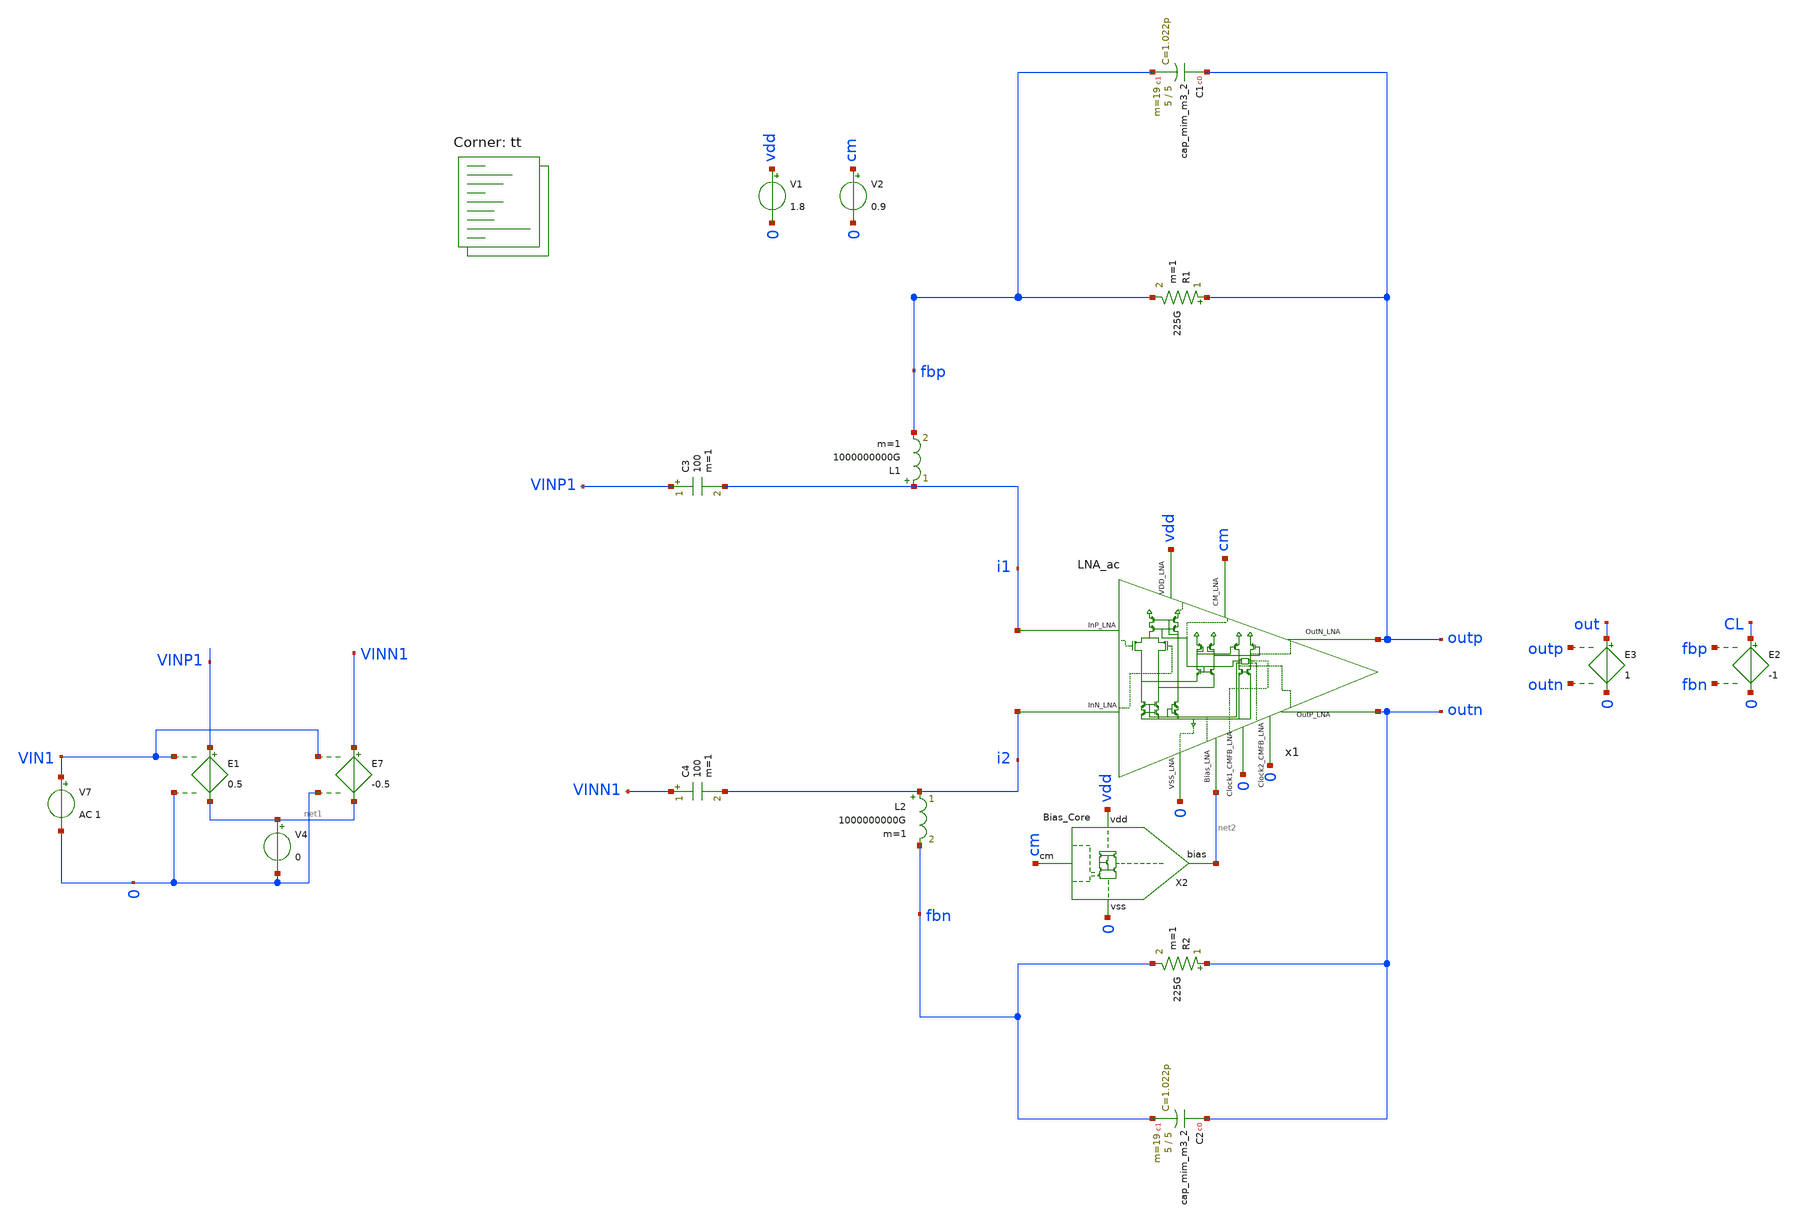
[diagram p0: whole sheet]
** sch_path: testbench_stability.sch
**.subckt testbench_stability
x1 i2 i1 vdd cm outp outn 0 net2 0 0 LNA_ac
V1 vdd 0 1.8
V2 cm 0 0.9
E1 VINP1 net1 VIN1 0 0.5
E7 VINN1 net1 VIN1 0 -0.5
V4 net1 0 0
V7 VIN1 0 AC 1
R1 outp fbp 225G m=1
XC1 outp fbp sky130_fd_pr__cap_mim_m3_2 W=5 L=5 MF=19 m=19
XC2 outn fbn sky130_fd_pr__cap_mim_m3_2 W=5 L=5 MF=19 m=19
R2 outn fbn 225G m=1
X2 cm vdd 0 net2 Bias_Core
E3 out 0 outp outn 1
L1 i1 fbp 1000000000G m=1
L2 i2 fbn 1000000000G m=1
E2 CL 0 fbp fbn -1
C3 VINP1 i1 100 m=1
C4 VINN1 i2 100 m=1
**** begin user architecture code
.lib $::SKYWATER_MODELS/sky130.lib.spice tt


.options savecurrents gmin=1e-25
*ic v(VM5)=0.9 v(VM6)=0.9
.control


save all

save @m.xm11.msky130_fd_pr__pfet_01v8_lvt[id]
save @m.xm11.msky130_fd_pr__pfet_01v8_lvt[vgs]


*nmos
save @m.xm3.msky130_fd_pr__nfet_01v8_lvt[vgs]
save @m.xm3.msky130_fd_pr__nfet_01v8_lvt[vth]
save @m.xm3.msky130_fd_pr__nfet_01v8_lvt[vds]

save @m.xm6.msky130_fd_pr__nfet_01v8_lvt[vgs]
save @m.xm6.msky130_fd_pr__nfet_01v8_lvt[vth]
save @m.xm6.msky130_fd_pr__nfet_01v8_lvt[vds]

save @m.xm8.msky130_fd_pr__nfet_01v8_lvt[vgs]
save @m.xm8.msky130_fd_pr__nfet_01v8_lvt[vth]
save @m.xm8.msky130_fd_pr__nfet_01v8_lvt[vds]

save @m.xm9.msky130_fd_pr__nfet_01v8_lvt[vgs]
save @m.xm9.msky130_fd_pr__nfet_01v8_lvt[vth]
save @m.xm9.msky130_fd_pr__nfet_01v8_lvt[vds]

save @m.xm18.msky130_fd_pr__nfet_01v8_lvt[vgs]
save @m.xm18.msky130_fd_pr__nfet_01v8_lvt[vth]
save @m.xm18.msky130_fd_pr__nfet_01v8_lvt[vds]

save @m.xm19.msky130_fd_pr__nfet_01v8_lvt[vgs]
save @m.xm19.msky130_fd_pr__nfet_01v8_lvt[vth]
save @m.xm19.msky130_fd_pr__nfet_01v8_lvt[vds]

save @m.xm25.msky130_fd_pr__nfet_01v8_lvt[vgs]
save @m.xm25.msky130_fd_pr__nfet_01v8_lvt[vth]
save @m.xm25.msky130_fd_pr__nfet_01v8_lvt[vds]

*pmos

save @m.xm1.msky130_fd_pr__pfet_01v8_lvt[vgs]
save @m.xm1.msky130_fd_pr__pfet_01v8_lvt[vth]
save @m.xm1.msky130_fd_pr__pfet_01v8_lvt[vds]


save @m.xm2.msky130_fd_pr__pfet_01v8_lvt[vgs]
save @m.xm2.msky130_fd_pr__pfet_01v8_lvt[vth]
save @m.xm2.msky130_fd_pr__pfet_01v8_lvt[vds]


save @m.xm10.msky130_fd_pr__pfet_01v8_lvt[vgs]
save @m.xm10.msky130_fd_pr__pfet_01v8_lvt[vth]
save @m.xm10.msky130_fd_pr__pfet_01v8_lvt[vds]

save @m.xm13.msky130_fd_pr__pfet_01v8_lvt[vgs]
save @m.xm13.msky130_fd_pr__pfet_01v8_lvt[vth]
save @m.xm13.msky130_fd_pr__pfet_01v8_lvt[vds]

save @m.xm4.msky130_fd_pr__pfet_01v8_lvt[vgs]
save @m.xm4.msky130_fd_pr__pfet_01v8_lvt[vth]
save @m.xm4.msky130_fd_pr__pfet_01v8_lvt[vds]

save @m.xm5.msky130_fd_pr__pfet_01v8_lvt[vgs]
save @m.xm5.msky130_fd_pr__pfet_01v8_lvt[vth]
save @m.xm5.msky130_fd_pr__pfet_01v8_lvt[vds]

save @m.xm16.msky130_fd_pr__pfet_01v8_lvt[vgs]
save @m.xm16.msky130_fd_pr__pfet_01v8_lvt[vth]
save @m.xm16.msky130_fd_pr__pfet_01v8_lvt[vds]

save @m.xm17.msky130_fd_pr__pfet_01v8_lvt[vgs]
save @m.xm17.msky130_fd_pr__pfet_01v8_lvt[vth]
save @m.xm17.msky130_fd_pr__pfet_01v8_lvt[vds]

save @m.xm3.msky130_fd_pr__pfet_01v8_lvt[vgs]
save @m.xm3.msky130_fd_pr__pfet_01v8_lvt[vth]
save @m.xm3.msky130_fd_pr__pfet_01v8_lvt[vds]

save @m.xm20.msky130_fd_pr__pfet_01v8_lvt[vgs]
save @m.xm20.msky130_fd_pr__pfet_01v8_lvt[vth]
save @m.xm20.msky130_fd_pr__pfet_01v8_lvt[vds]

save @m.xm2.msky130_fd_pr__pfet_01v8_lvt[vgs]
save @m.xm2.msky130_fd_pr__pfet_01v8_lvt[vth]
save @m.xm2.msky130_fd_pr__pfet_01v8_lvt[vds]

save @m.xm21.msky130_fd_pr__pfet_01v8_lvt[vgs]
save @m.xm21.msky130_fd_pr__pfet_01v8_lvt[vth]
save @m.xm21.msky130_fd_pr__pfet_01v8_lvt[vds]

save @m.xm7.msky130_fd_pr__nfet_01v8_lvt[vth]

save @m.xm1.msky130_fd_pr__pfet_01v8[vgs]

save @m.xm1.msky130_fd_pr__nfet_01v8_lvt[gm]


save @m.xm1.msky130_fd_pr__nfet_01v8_lvt[gds]
save @m.xm2.msky130_fd_pr__pfet_01v8_lvt[gm]

save @m.xm23.msky130_fd_pr__nfet_01v8[cgs]
save @m.xm4.msky130_fd_pr__pfet_01v8[cgs]
save @m.xm2.msky130_fd_pr__pfet_01v8_lvt[cgs]



save @m.xm2.msky130_fd_pr__pfet_01v8_lvt[gds]


op
write CL_Stability.raw
*set appendwrite


.endc
.control



*tran 50u 1500m
*save all
*plot v(Outp)-v(outn)


*noise V(Outp,Outn) V7 dec 100 0.1 128
*print inoise_total onoise_total
*setplot noise1
*plot inoise_spectrum

ac dec 10 0.1 1G
let gaind=(v(outp)-v(outn))/(v(in_p1)-v(in_n1))
let lg=fbp-fbn
let BG=(OL/CL)-1
let phase=180*cph(CL)/pi
plot db(gaind)
plot db(CL) phase
plot db(out)

.endc






.include $::SKYWATER_STDCELLS/sky130_fd_sc_hd.spice

**** end user architecture code
**.ends

* expanding   symbol:  LNA/LNA_ac.sym # of pins=10
** sym_path: LNA_ac.sym
** sch_path: LNA_ac.sch
.subckt LNA_ac InN_LNA InP_LNA VDD_LNA CM_LNA OutN_LNA OutP_LNA VSS_LNA Bias_LNA Clock1_CMFB_LNA
+ Clock2_CMFB_LNA
*.iopin InP_LNA
*.iopin InN_LNA
*.iopin VSS_LNA
*.iopin VDD_LNA
*.iopin CM_LNA
*.opin OutP_LNA
*.opin OutN_LNA
*.iopin Clock2_CMFB_LNA
*.iopin Bias_LNA
*.iopin Clock1_CMFB_LNA
XM4 net4 InP_LNA VT2 VT2 sky130_fd_pr__pfet_01v8_lvt L=10 W=10 nf=1 ad='int((nf+1)/2) * W/nf * 0.29'
+ as='int((nf+2)/2) * W/nf * 0.29' pd='2*int((nf+1)/2) * (W/nf + 0.29)' ps='2*int((nf+2)/2) * (W/nf + 0.29)'
+ nrd='0.29 / W' nrs='0.29 / W' sa=0 sb=0 sd=0 mult=45 m=45
XM5 net3 InN_LNA VT2 VT2 sky130_fd_pr__pfet_01v8_lvt L=10 W=10 nf=1 ad='int((nf+1)/2) * W/nf * 0.29'
+ as='int((nf+2)/2) * W/nf * 0.29' pd='2*int((nf+1)/2) * (W/nf + 0.29)' ps='2*int((nf+2)/2) * (W/nf + 0.29)'
+ nrd='0.29 / W' nrs='0.29 / W' sa=0 sb=0 sd=0 mult=45 m=45
XM8 net8 Bias_LNA VSS_LNA VSS_LNA sky130_fd_pr__nfet_01v8_lvt L=20 W=10 nf=1 ad='int((nf+1)/2) * W/nf * 0.29'
+ as='int((nf+2)/2) * W/nf * 0.29' pd='2*int((nf+1)/2) * (W/nf + 0.29)' ps='2*int((nf+2)/2) * (W/nf + 0.29)'
+ nrd='0.29 / W' nrs='0.29 / W' sa=0 sb=0 sd=0 mult=3 m=3
XM9 net9 Bias_LNA VSS_LNA VSS_LNA sky130_fd_pr__nfet_01v8_lvt L=20 W=10 nf=1 ad='int((nf+1)/2) * W/nf * 0.29'
+ as='int((nf+2)/2) * W/nf * 0.29' pd='2*int((nf+1)/2) * (W/nf + 0.29)' ps='2*int((nf+2)/2) * (W/nf + 0.29)'
+ nrd='0.29 / W' nrs='0.29 / W' sa=0 sb=0 sd=0 mult=3 m=3
XM16 net7 b VDD_LNA VDD_LNA sky130_fd_pr__pfet_01v8_lvt L=20 W=6 nf=1 ad='int((nf+1)/2) * W/nf * 0.29'
+ as='int((nf+2)/2) * W/nf * 0.29' pd='2*int((nf+1)/2) * (W/nf + 0.29)' ps='2*int((nf+2)/2) * (W/nf + 0.29)'
+ nrd='0.29 / W' nrs='0.29 / W' sa=0 sb=0 sd=0 mult=1 m=1
XM17 net6 a VDD_LNA VDD_LNA sky130_fd_pr__pfet_01v8_lvt L=20 W=6 nf=1 ad='int((nf+1)/2) * W/nf * 0.29'
+ as='int((nf+2)/2) * W/nf * 0.29' pd='2*int((nf+1)/2) * (W/nf + 0.29)' ps='2*int((nf+2)/2) * (W/nf + 0.29)'
+ nrd='0.29 / W' nrs='0.29 / W' sa=0 sb=0 sd=0 mult=1 m=1
XM18 b CM_LNA net3 VSS_LNA sky130_fd_pr__nfet_01v8_lvt L=20 W=1 nf=1 ad='int((nf+1)/2) * W/nf * 0.29'
+ as='int((nf+2)/2) * W/nf * 0.29' pd='2*int((nf+1)/2) * (W/nf + 0.29)' ps='2*int((nf+2)/2) * (W/nf + 0.29)'
+ nrd='0.29 / W' nrs='0.29 / W' sa=0 sb=0 sd=0 mult=12 m=12
XM19 a CM_LNA net4 VSS_LNA sky130_fd_pr__nfet_01v8_lvt L=20 W=1 nf=1 ad='int((nf+1)/2) * W/nf * 0.29'
+ as='int((nf+2)/2) * W/nf * 0.29' pd='2*int((nf+1)/2) * (W/nf + 0.29)' ps='2*int((nf+2)/2) * (W/nf + 0.29)'
+ nrd='0.29 / W' nrs='0.29 / W' sa=0 sb=0 sd=0 mult=12 m=12
XM20 OutP_LNA a VDD_LNA VDD_LNA sky130_fd_pr__pfet_01v8_lvt L=20 W=6 nf=1 ad='int((nf+1)/2) * W/nf * 0.29'
+ as='int((nf+2)/2) * W/nf * 0.29' pd='2*int((nf+1)/2) * (W/nf + 0.29)' ps='2*int((nf+2)/2) * (W/nf + 0.29)'
+ nrd='0.29 / W' nrs='0.29 / W' sa=0 sb=0 sd=0 mult=10 m=10
XM21 OutN_LNA b VDD_LNA VDD_LNA sky130_fd_pr__pfet_01v8_lvt L=20 W=6 nf=1 ad='int((nf+1)/2) * W/nf * 0.29'
+ as='int((nf+2)/2) * W/nf * 0.29' pd='2*int((nf+1)/2) * (W/nf + 0.29)' ps='2*int((nf+2)/2) * (W/nf + 0.29)'
+ nrd='0.29 / W' nrs='0.29 / W' sa=0 sb=0 sd=0 mult=10 m=10
XM23 OutN_LNA net5 VSS_LNA VSS_LNA sky130_fd_pr__nfet_01v8_lvt L=20 W=10 nf=1 ad='int((nf+1)/2) * W/nf * 0.29'
+ as='int((nf+2)/2) * W/nf * 0.29' pd='2*int((nf+1)/2) * (W/nf + 0.29)' ps='2*int((nf+2)/2) * (W/nf + 0.29)'
+ nrd='0.29 / W' nrs='0.29 / W' sa=0 sb=0 sd=0 mult=10 m=10
XM25 OutP_LNA net5 VSS_LNA VSS_LNA sky130_fd_pr__nfet_01v8_lvt L=20 W=10 nf=1 ad='int((nf+1)/2) * W/nf * 0.29'
+ as='int((nf+2)/2) * W/nf * 0.29' pd='2*int((nf+1)/2) * (W/nf + 0.29)' ps='2*int((nf+2)/2) * (W/nf + 0.29)'
+ nrd='0.29 / W' nrs='0.29 / W' sa=0 sb=0 sd=0 mult=10 m=10
XM2 net10 net1 VDD_LNA VDD_LNA sky130_fd_pr__pfet_01v8_lvt L=10 W=10 nf=1 ad='int((nf+1)/2) * W/nf * 0.29'
+ as='int((nf+2)/2) * W/nf * 0.29' pd='2*int((nf+1)/2) * (W/nf + 0.29)' ps='2*int((nf+2)/2) * (W/nf + 0.29)'
+ nrd='0.29 / W' nrs='0.29 / W' sa=0 sb=0 sd=0 mult=4 m=4
XM3 net11 net1 VDD_LNA VDD_LNA sky130_fd_pr__pfet_01v8_lvt L=10 W=10 nf=1 ad='int((nf+1)/2) * W/nf * 0.29'
+ as='int((nf+2)/2) * W/nf * 0.29' pd='2*int((nf+1)/2) * (W/nf + 0.29)' ps='2*int((nf+2)/2) * (W/nf + 0.29)'
+ nrd='0.29 / W' nrs='0.29 / W' sa=0 sb=0 sd=0 mult=1 m=1
XM6 net2 Bias_LNA VSS_LNA VSS_LNA sky130_fd_pr__nfet_01v8_lvt L=20 W=10 nf=1 ad='int((nf+1)/2) * W/nf * 0.29'
+ as='int((nf+2)/2) * W/nf * 0.29' pd='2*int((nf+1)/2) * (W/nf + 0.29)' ps='2*int((nf+2)/2) * (W/nf + 0.29)'
+ nrd='0.29 / W' nrs='0.29 / W' sa=0 sb=0 sd=0 mult=1 m=1
E3 f1 VSS_LNA OutN_LNA VSS_LNA -1
E4 f2 VSS_LNA OutP_LNA f1 1
E5 f3 VSS_LNA f2 VSS_LNA 0.5
E6 net5 VSS_LNA CM_LNA f3 {-1000}
XC1 OutP_LNA a sky130_fd_pr__cap_mim_m3_2 W=12 L=10 MF=32 m=32
XC2 OutN_LNA b sky130_fd_pr__cap_mim_m3_2 W=12 L=10 MF=32 m=32
XM1 net4 CM_LNA net8 VSS_LNA sky130_fd_pr__nfet_01v8_lvt L=1 W=10 nf=1 ad='int((nf+1)/2) * W/nf * 0.29'
+ as='int((nf+2)/2) * W/nf * 0.29' pd='2*int((nf+1)/2) * (W/nf + 0.29)' ps='2*int((nf+2)/2) * (W/nf + 0.29)'
+ nrd='0.29 / W' nrs='0.29 / W' sa=0 sb=0 sd=0 mult=120 m=120
XM7 net3 CM_LNA net9 VSS_LNA sky130_fd_pr__nfet_01v8_lvt L=1 W=10 nf=1 ad='int((nf+1)/2) * W/nf * 0.29'
+ as='int((nf+2)/2) * W/nf * 0.29' pd='2*int((nf+1)/2) * (W/nf + 0.29)' ps='2*int((nf+2)/2) * (W/nf + 0.29)'
+ nrd='0.29 / W' nrs='0.29 / W' sa=0 sb=0 sd=0 mult=120 m=120
XM10 net1 CM_LNA net2 VSS_LNA sky130_fd_pr__nfet_01v8_lvt L=1 W=10 nf=1 ad='int((nf+1)/2) * W/nf * 0.29'
+ as='int((nf+2)/2) * W/nf * 0.29' pd='2*int((nf+1)/2) * (W/nf + 0.29)' ps='2*int((nf+2)/2) * (W/nf + 0.29)'
+ nrd='0.29 / W' nrs='0.29 / W' sa=0 sb=0 sd=0 mult=40 m=40
XM11 net1 CM_LNA net11 VDD_LNA sky130_fd_pr__pfet_01v8_lvt L=10 W=10 nf=1 ad='int((nf+1)/2) * W/nf * 0.29'
+ as='int((nf+2)/2) * W/nf * 0.29' pd='2*int((nf+1)/2) * (W/nf + 0.29)' ps='2*int((nf+2)/2) * (W/nf + 0.29)'
+ nrd='0.29 / W' nrs='0.29 / W' sa=0 sb=0 sd=0 mult=5 m=5
XM12 VT2 CM_LNA net10 VDD_LNA sky130_fd_pr__pfet_01v8_lvt L=10 W=10 nf=1 ad='int((nf+1)/2) * W/nf * 0.29'
+ as='int((nf+2)/2) * W/nf * 0.29' pd='2*int((nf+1)/2) * (W/nf + 0.29)' ps='2*int((nf+2)/2) * (W/nf + 0.29)'
+ nrd='0.29 / W' nrs='0.29 / W' sa=0 sb=0 sd=0 mult=20 m=20
XM13 b CM_LNA net7 VDD_LNA sky130_fd_pr__pfet_01v8_lvt L=20 W=6 nf=1 ad='int((nf+1)/2) * W/nf * 0.29'
+ as='int((nf+2)/2) * W/nf * 0.29' pd='2*int((nf+1)/2) * (W/nf + 0.29)' ps='2*int((nf+2)/2) * (W/nf + 0.29)'
+ nrd='0.29 / W' nrs='0.29 / W' sa=0 sb=0 sd=0 mult=10 m=10
XM14 a CM_LNA net6 VDD_LNA sky130_fd_pr__pfet_01v8_lvt L=20 W=6 nf=1 ad='int((nf+1)/2) * W/nf * 0.29'
+ as='int((nf+2)/2) * W/nf * 0.29' pd='2*int((nf+1)/2) * (W/nf + 0.29)' ps='2*int((nf+2)/2) * (W/nf + 0.29)'
+ nrd='0.29 / W' nrs='0.29 / W' sa=0 sb=0 sd=0 mult=10 m=10
.ends


* expanding   symbol:  LNA/Bias_Core.sym # of pins=4
** sym_path: Bias_Core.sym
** sch_path: Bias_Core.sch
.subckt Bias_Core cm vdd vss bias
*.ipin vdd
*.ipin vss
*.opin bias
*.ipin cm
XM7 net3 bias vss vss sky130_fd_pr__nfet_01v8_lvt L=20 W=10 nf=1 ad='int((nf+1)/2) * W/nf * 0.29' as='int((nf+2)/2) * W/nf * 0.29'
+ pd='2*int((nf+1)/2) * (W/nf + 0.29)' ps='2*int((nf+2)/2) * (W/nf + 0.29)' nrd='0.29 / W' nrs='0.29 / W'
+ sa=0 sb=0 sd=0 mult=1 m=1
XM10 net4 vx vr vdd sky130_fd_pr__pfet_01v8_lvt L=20 W=10 nf=1 ad='int((nf+1)/2) * W/nf * 0.29' as='int((nf+2)/2) * W/nf * 0.29'
+ pd='2*int((nf+1)/2) * (W/nf + 0.29)' ps='2*int((nf+2)/2) * (W/nf + 0.29)' nrd='0.29 / W' nrs='0.29 / W'
+ sa=0 sb=0 sd=0 mult=20 m=20
XM11 bias cm net3 vss sky130_fd_pr__nfet_01v8_lvt L=20 W=10 nf=1 ad='int((nf+1)/2) * W/nf * 0.29' as='int((nf+2)/2) * W/nf * 0.29'
+ pd='2*int((nf+1)/2) * (W/nf + 0.29)' ps='2*int((nf+2)/2) * (W/nf + 0.29)' nrd='0.29 / W' nrs='0.29 / W'
+ sa=0 sb=0 sd=0 mult=40 m=40
XM12 net2 bias vss vss sky130_fd_pr__nfet_01v8_lvt L=20 W=10 nf=1 ad='int((nf+1)/2) * W/nf * 0.29' as='int((nf+2)/2) * W/nf * 0.29'
+ pd='2*int((nf+1)/2) * (W/nf + 0.29)' ps='2*int((nf+2)/2) * (W/nf + 0.29)' nrd='0.29 / W' nrs='0.29 / W'
+ sa=0 sb=0 sd=0 mult=1 m=1
XM13 vx cm net2 vss sky130_fd_pr__nfet_01v8_lvt L=20 W=10 nf=1 ad='int((nf+1)/2) * W/nf * 0.29' as='int((nf+2)/2) * W/nf * 0.29'
+ pd='2*int((nf+1)/2) * (W/nf + 0.29)' ps='2*int((nf+2)/2) * (W/nf + 0.29)' nrd='0.29 / W' nrs='0.29 / W'
+ sa=0 sb=0 sd=0 mult=40 m=40
XM2 net8 vx net1 vdd sky130_fd_pr__pfet_01v8_lvt L=20 W=10 nf=1 ad='int((nf+1)/2) * W/nf * 0.29' as='int((nf+2)/2) * W/nf * 0.29'
+ pd='2*int((nf+1)/2) * (W/nf + 0.29)' ps='2*int((nf+2)/2) * (W/nf + 0.29)' nrd='0.29 / W' nrs='0.29 / W'
+ sa=0 sb=0 sd=0 mult=20 m=20
XM3 net1 net1 vdd vdd sky130_fd_pr__pfet_01v8_lvt L=1 W=10 nf=1 ad='int((nf+1)/2) * W/nf * 0.29' as='int((nf+2)/2) * W/nf * 0.29'
+ pd='2*int((nf+1)/2) * (W/nf + 0.29)' ps='2*int((nf+2)/2) * (W/nf + 0.29)' nrd='0.29 / W' nrs='0.29 / W'
+ sa=0 sb=0 sd=0 mult=6 m=6
XM4 net5 net5 bias vss sky130_fd_pr__nfet_01v8_lvt L=10 W=1 nf=1 ad='int((nf+1)/2) * W/nf * 0.29' as='int((nf+2)/2) * W/nf * 0.29'
+ pd='2*int((nf+1)/2) * (W/nf + 0.29)' ps='2*int((nf+2)/2) * (W/nf + 0.29)' nrd='0.29 / W' nrs='0.29 / W'
+ sa=0 sb=0 sd=0 mult=1 m=1
XM5 net6 net6 net5 vss sky130_fd_pr__nfet_01v8_lvt L=10 W=1 nf=1 ad='int((nf+1)/2) * W/nf * 0.29' as='int((nf+2)/2) * W/nf * 0.29'
+ pd='2*int((nf+1)/2) * (W/nf + 0.29)' ps='2*int((nf+2)/2) * (W/nf + 0.29)' nrd='0.29 / W' nrs='0.29 / W'
+ sa=0 sb=0 sd=0 mult=1 m=1
XM8 net7 net7 net6 vss sky130_fd_pr__nfet_01v8_lvt L=10 W=1 nf=1 ad='int((nf+1)/2) * W/nf * 0.29' as='int((nf+2)/2) * W/nf * 0.29'
+ pd='2*int((nf+1)/2) * (W/nf + 0.29)' ps='2*int((nf+2)/2) * (W/nf + 0.29)' nrd='0.29 / W' nrs='0.29 / W'
+ sa=0 sb=0 sd=0 mult=1 m=1
XM9 vx vx net7 vss sky130_fd_pr__nfet_01v8_lvt L=10 W=1 nf=1 ad='int((nf+1)/2) * W/nf * 0.29' as='int((nf+2)/2) * W/nf * 0.29'
+ pd='2*int((nf+1)/2) * (W/nf + 0.29)' ps='2*int((nf+2)/2) * (W/nf + 0.29)' nrd='0.29 / W' nrs='0.29 / W'
+ sa=0 sb=0 sd=0 mult=1 m=1
XM23 bias vx net4 vdd sky130_fd_pr__pfet_01v8_lvt L=20 W=10 nf=1 ad='int((nf+1)/2) * W/nf * 0.29' as='int((nf+2)/2) * W/nf * 0.29'
+ pd='2*int((nf+1)/2) * (W/nf + 0.29)' ps='2*int((nf+2)/2) * (W/nf + 0.29)' nrd='0.29 / W' nrs='0.29 / W'
+ sa=0 sb=0 sd=0 mult=5 m=5
XM24 vx vx net8 vdd sky130_fd_pr__pfet_01v8_lvt L=20 W=10 nf=1 ad='int((nf+1)/2) * W/nf * 0.29' as='int((nf+2)/2) * W/nf * 0.29'
+ pd='2*int((nf+1)/2) * (W/nf + 0.29)' ps='2*int((nf+2)/2) * (W/nf + 0.29)' nrd='0.29 / W' nrs='0.29 / W'
+ sa=0 sb=0 sd=0 mult=5 m=5
R27 vdd vr 3e6 m=1
.ends

.end
